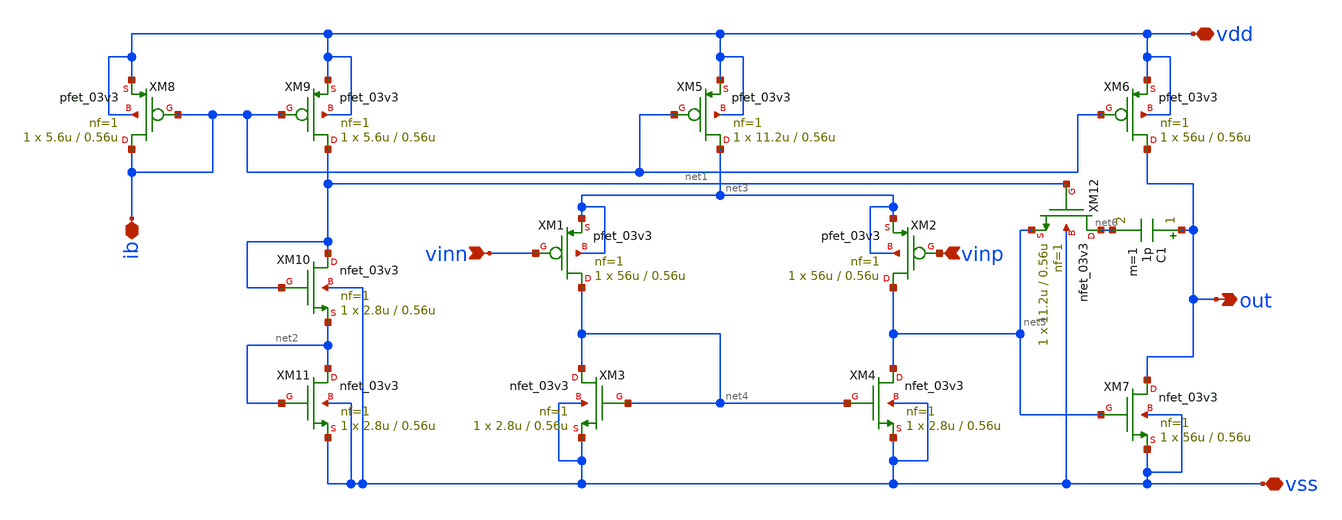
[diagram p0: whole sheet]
** sch_path: opamp_03v3.sch
**.subckt opamp_03v3 ib vdd vinn out vss vinp
*.iopin ib
*.iopin vdd
*.ipin vinn
*.opin out
*.iopin vss
*.ipin vinp
XM1 net4 vinn net3 net3 pfet_03v3 L=0.56u W=56u nf=1 ad='int((nf+1)/2) * W/nf * 0.18u' as='int((nf+2)/2) * W/nf * 0.18u'
+ pd='2*int((nf+1)/2) * (W/nf + 0.18u)' ps='2*int((nf+2)/2) * (W/nf + 0.18u)' nrd='0.18u / W' nrs='0.18u / W'
+ sa=0 sb=0 sd=0 m=1
XM2 net5 vinp net3 net3 pfet_03v3 L=0.56u W=56u nf=1 ad='int((nf+1)/2) * W/nf * 0.18u' as='int((nf+2)/2) * W/nf * 0.18u'
+ pd='2*int((nf+1)/2) * (W/nf + 0.18u)' ps='2*int((nf+2)/2) * (W/nf + 0.18u)' nrd='0.18u / W' nrs='0.18u / W'
+ sa=0 sb=0 sd=0 m=1
XM3 net4 net4 vss vss nfet_03v3 L=0.56u W=2.8u nf=1 ad='int((nf+1)/2) * W/nf * 0.18u' as='int((nf+2)/2) * W/nf * 0.18u'
+ pd='2*int((nf+1)/2) * (W/nf + 0.18u)' ps='2*int((nf+2)/2) * (W/nf + 0.18u)' nrd='0.18u / W' nrs='0.18u / W'
+ sa=0 sb=0 sd=0 m=1
XM4 net5 net4 vss vss nfet_03v3 L=0.56u W=2.8u nf=1 ad='int((nf+1)/2) * W/nf * 0.18u' as='int((nf+2)/2) * W/nf * 0.18u'
+ pd='2*int((nf+1)/2) * (W/nf + 0.18u)' ps='2*int((nf+2)/2) * (W/nf + 0.18u)' nrd='0.18u / W' nrs='0.18u / W'
+ sa=0 sb=0 sd=0 m=1
XM5 net3 ib vdd vdd pfet_03v3 L=0.56u W=11.2u nf=1 ad='int((nf+1)/2) * W/nf * 0.18u' as='int((nf+2)/2) * W/nf * 0.18u'
+ pd='2*int((nf+1)/2) * (W/nf + 0.18u)' ps='2*int((nf+2)/2) * (W/nf + 0.18u)' nrd='0.18u / W' nrs='0.18u / W'
+ sa=0 sb=0 sd=0 m=1
XM6 out ib vdd vdd pfet_03v3 L=0.56u W=56u nf=1 ad='int((nf+1)/2) * W/nf * 0.18u' as='int((nf+2)/2) * W/nf * 0.18u'
+ pd='2*int((nf+1)/2) * (W/nf + 0.18u)' ps='2*int((nf+2)/2) * (W/nf + 0.18u)' nrd='0.18u / W' nrs='0.18u / W'
+ sa=0 sb=0 sd=0 m=1
XM7 out net5 vss vss nfet_03v3 L=0.56u W=56u nf=1 ad='int((nf+1)/2) * W/nf * 0.18u' as='int((nf+2)/2) * W/nf * 0.18u'
+ pd='2*int((nf+1)/2) * (W/nf + 0.18u)' ps='2*int((nf+2)/2) * (W/nf + 0.18u)' nrd='0.18u / W' nrs='0.18u / W'
+ sa=0 sb=0 sd=0 m=1
C1 out net6 1p m=1
XM8 ib ib vdd vdd pfet_03v3 L=0.56u W=5.6u nf=1 ad='int((nf+1)/2) * W/nf * 0.18u' as='int((nf+2)/2) * W/nf * 0.18u'
+ pd='2*int((nf+1)/2) * (W/nf + 0.18u)' ps='2*int((nf+2)/2) * (W/nf + 0.18u)' nrd='0.18u / W' nrs='0.18u / W'
+ sa=0 sb=0 sd=0 m=1
XM9 net1 ib vdd vdd pfet_03v3 L=0.56u W=5.6u nf=1 ad='int((nf+1)/2) * W/nf * 0.18u' as='int((nf+2)/2) * W/nf * 0.18u'
+ pd='2*int((nf+1)/2) * (W/nf + 0.18u)' ps='2*int((nf+2)/2) * (W/nf + 0.18u)' nrd='0.18u / W' nrs='0.18u / W'
+ sa=0 sb=0 sd=0 m=1
XM10 net1 net1 net2 vss nfet_03v3 L=0.56u W=2.8u nf=1 ad='int((nf+1)/2) * W/nf * 0.18u' as='int((nf+2)/2) * W/nf * 0.18u'
+ pd='2*int((nf+1)/2) * (W/nf + 0.18u)' ps='2*int((nf+2)/2) * (W/nf + 0.18u)' nrd='0.18u / W' nrs='0.18u / W'
+ sa=0 sb=0 sd=0 m=1
XM11 net2 net2 vss vss nfet_03v3 L=0.56u W=2.8u nf=1 ad='int((nf+1)/2) * W/nf * 0.18u' as='int((nf+2)/2) * W/nf * 0.18u'
+ pd='2*int((nf+1)/2) * (W/nf + 0.18u)' ps='2*int((nf+2)/2) * (W/nf + 0.18u)' nrd='0.18u / W' nrs='0.18u / W'
+ sa=0 sb=0 sd=0 m=1
XM12 net6 net1 net5 vss nfet_03v3 L=0.56u W=11.2u nf=1 ad='int((nf+1)/2) * W/nf * 0.18u' as='int((nf+2)/2) * W/nf * 0.18u'
+ pd='2*int((nf+1)/2) * (W/nf + 0.18u)' ps='2*int((nf+2)/2) * (W/nf + 0.18u)' nrd='0.18u / W' nrs='0.18u / W'
+ sa=0 sb=0 sd=0 m=1
**.ends
.end
